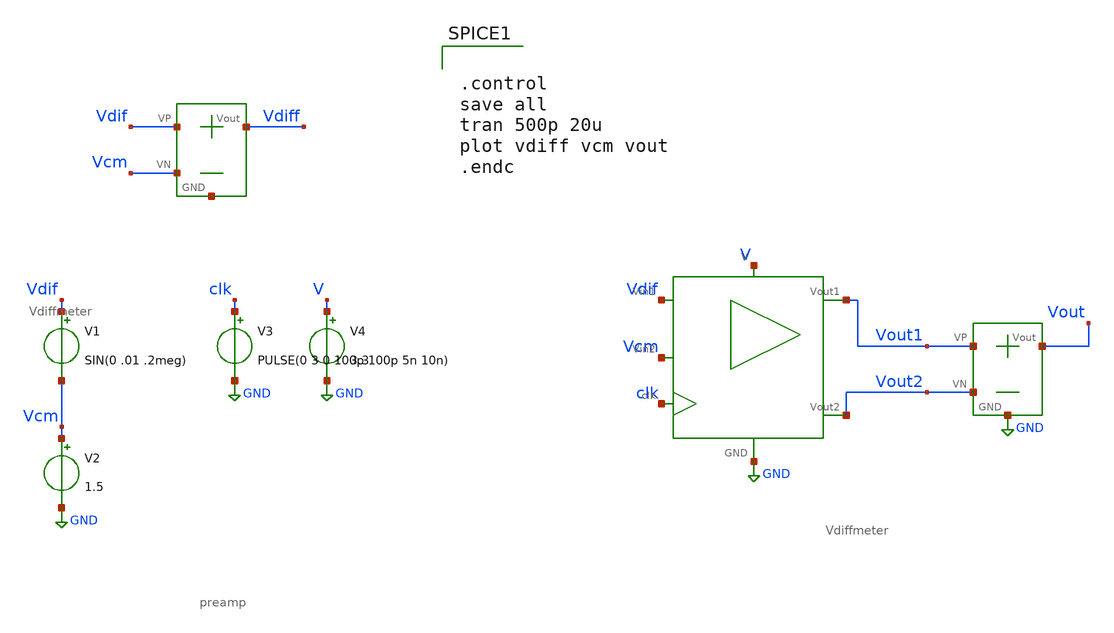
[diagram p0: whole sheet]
** sch_path: SAR_ADC/xschem/test/preamp_tb/vdif_sin-vcm_DC__tb.sch
**.subckt vdif_sin-vcm_DC__tb
V1 Vdif Vcm SIN(0 .01 .2meg)
V2 Vcm GND 1.5
V3 clk GND PULSE(0 3 0 100p 100p 5n 10n)
V4 V GND 3.3
X1 V GND Vdif clk Vout1 Vout2 Vcm preamp
X3 Vout1 Vout2 Vout GND Vdiffmeter
X2 Vdif Vcm Vdiff net1 Vdiffmeter
**** begin user architecture code


.control
save all
tran 500p 20u
plot vdiff vcm vout
.endc


.include /foss/pdks/gf180mcuC/libs.tech/ngspice/design.ngspice
.lib /foss/pdks/gf180mcuC/libs.tech/ngspice/sm141064.ngspice typical

**** end user architecture code
**.ends
.GLOBAL GND
.end
